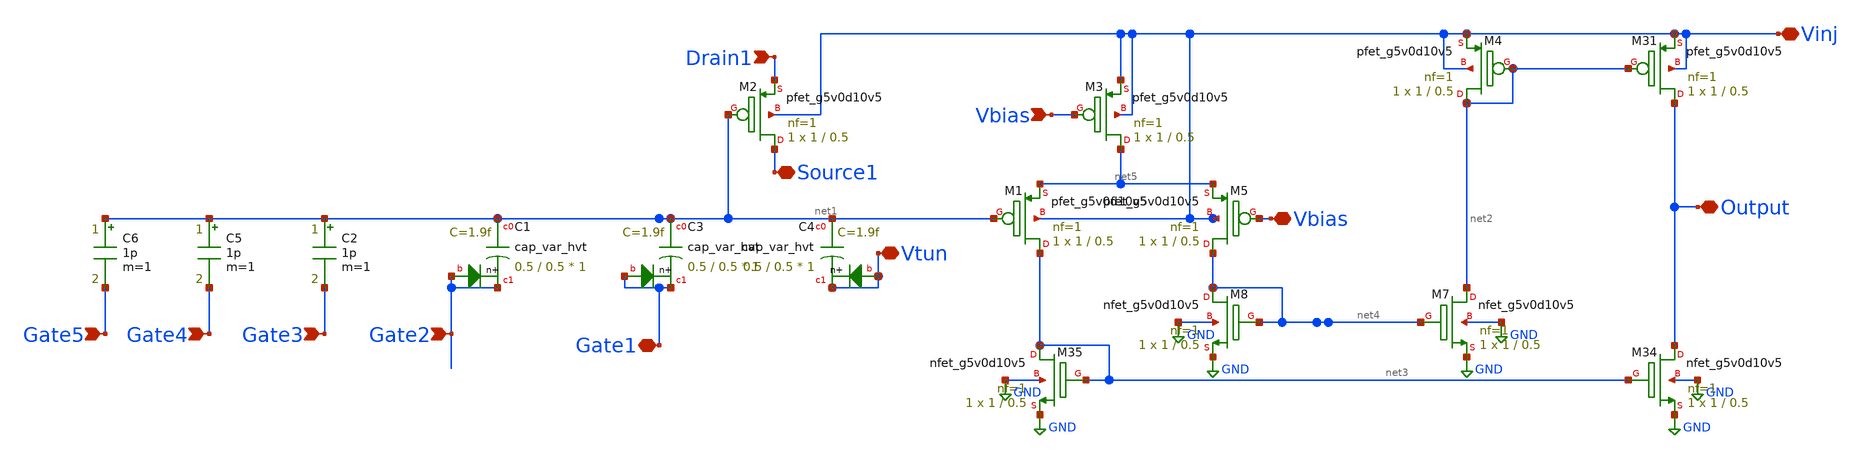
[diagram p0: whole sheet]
** sch_path: libs.ref/sky130_hilas_sc/xschem/sky130_hilas_FGcharacterization01.sch
**.subckt sky130_hilas_FGcharacterization01 Vbias Drain1 Gate3 Gate2 Vtun Source1 Vinj Gate1 Output
*+ Vbias Gate4 Gate5
*.ipin Vbias
*.ipin Drain1
*.ipin Gate3
*.ipin Gate2
*.iopin Vtun
*.iopin Source1
*.iopin Vinj
*.iopin Gate1
*.iopin Output
*.iopin Vbias
*.ipin Gate4
*.ipin Gate5
XM3 net5 Vbias Vinj Vinj sky130_fd_pr__pfet_g5v0d10v5 L=0.5 W=1 nf=1 ad='int((nf+1)/2) * W/nf * 0.29'
+ as='int((nf+2)/2) * W/nf * 0.29' pd='2*int((nf+1)/2) * (W/nf + 0.29)' ps='2*int((nf+2)/2) * (W/nf + 0.29)'
+ nrd='0.29 / W' nrs='0.29 / W' sa=0 sb=0 sd=0 mult=1 m=1
XC1 net1 Gate2 Gate2 sky130_fd_pr__cap_var_hvt W=0.5 L=0.5 VM=1 m=1
XM5 net4 Vbias net5 Vinj sky130_fd_pr__pfet_g5v0d10v5 L=0.5 W=1 nf=1 ad='int((nf+1)/2) * W/nf * 0.29'
+ as='int((nf+2)/2) * W/nf * 0.29' pd='2*int((nf+1)/2) * (W/nf + 0.29)' ps='2*int((nf+2)/2) * (W/nf + 0.29)'
+ nrd='0.29 / W' nrs='0.29 / W' sa=0 sb=0 sd=0 mult=1 m=1
XM1 net3 net1 net5 Vinj sky130_fd_pr__pfet_g5v0d10v5 L=0.5 W=1 nf=1 ad='int((nf+1)/2) * W/nf * 0.29'
+ as='int((nf+2)/2) * W/nf * 0.29' pd='2*int((nf+1)/2) * (W/nf + 0.29)' ps='2*int((nf+2)/2) * (W/nf + 0.29)'
+ nrd='0.29 / W' nrs='0.29 / W' sa=0 sb=0 sd=0 mult=1 m=1
XM2 Source1 net1 Drain1 Vinj sky130_fd_pr__pfet_g5v0d10v5 L=0.5 W=1 nf=1 ad='int((nf+1)/2) * W/nf * 0.29'
+ as='int((nf+2)/2) * W/nf * 0.29' pd='2*int((nf+1)/2) * (W/nf + 0.29)' ps='2*int((nf+2)/2) * (W/nf + 0.29)'
+ nrd='0.29 / W' nrs='0.29 / W' sa=0 sb=0 sd=0 mult=1 m=1
XC3 net1 Gate1 Gate1 sky130_fd_pr__cap_var_hvt W=0.5 L=0.5 VM=1 m=1
XM4 net2 net2 Vinj Vinj sky130_fd_pr__pfet_g5v0d10v5 L=0.5 W=1 nf=1 ad='int((nf+1)/2) * W/nf * 0.29'
+ as='int((nf+2)/2) * W/nf * 0.29' pd='2*int((nf+1)/2) * (W/nf + 0.29)' ps='2*int((nf+2)/2) * (W/nf + 0.29)'
+ nrd='0.29 / W' nrs='0.29 / W' sa=0 sb=0 sd=0 mult=1 m=1
XC4 net1 Vtun Vtun sky130_fd_pr__cap_var_hvt W=0.5 L=0.5 VM=1 m=1
XM31 Output net2 Vinj Vinj sky130_fd_pr__pfet_g5v0d10v5 L=0.5 W=1 nf=1 ad='int((nf+1)/2) * W/nf * 0.29'
+ as='int((nf+2)/2) * W/nf * 0.29' pd='2*int((nf+1)/2) * (W/nf + 0.29)' ps='2*int((nf+2)/2) * (W/nf + 0.29)'
+ nrd='0.29 / W' nrs='0.29 / W' sa=0 sb=0 sd=0 mult=1 m=1
XM34 Output net3 GND GND sky130_fd_pr__nfet_g5v0d10v5 L=0.5 W=1 nf=1 ad='int((nf+1)/2) * W/nf * 0.29'
+ as='int((nf+2)/2) * W/nf * 0.29' pd='2*int((nf+1)/2) * (W/nf + 0.29)' ps='2*int((nf+2)/2) * (W/nf + 0.29)'
+ nrd='0.29 / W' nrs='0.29 / W' sa=0 sb=0 sd=0 mult=1 m=1
XM35 net3 net3 GND GND sky130_fd_pr__nfet_g5v0d10v5 L=0.5 W=1 nf=1 ad='int((nf+1)/2) * W/nf * 0.29' as='int((nf+2)/2) * W/nf * 0.29'
+ pd='2*int((nf+1)/2) * (W/nf + 0.29)' ps='2*int((nf+2)/2) * (W/nf + 0.29)' nrd='0.29 / W' nrs='0.29 / W'
+ sa=0 sb=0 sd=0 mult=1 m=1
XM7 net2 net4 GND GND sky130_fd_pr__nfet_g5v0d10v5 L=0.5 W=1 nf=1 ad='int((nf+1)/2) * W/nf * 0.29' as='int((nf+2)/2) * W/nf * 0.29'
+ pd='2*int((nf+1)/2) * (W/nf + 0.29)' ps='2*int((nf+2)/2) * (W/nf + 0.29)' nrd='0.29 / W' nrs='0.29 / W'
+ sa=0 sb=0 sd=0 mult=1 m=1
XM8 net4 net4 GND GND sky130_fd_pr__nfet_g5v0d10v5 L=0.5 W=1 nf=1 ad='int((nf+1)/2) * W/nf * 0.29' as='int((nf+2)/2) * W/nf * 0.29'
+ pd='2*int((nf+1)/2) * (W/nf + 0.29)' ps='2*int((nf+2)/2) * (W/nf + 0.29)' nrd='0.29 / W' nrs='0.29 / W'
+ sa=0 sb=0 sd=0 mult=1 m=1
C2 net1 Gate3 1p m=1
C5 net1 Gate4 1p m=1
C6 net1 Gate5 1p m=1
**.ends
.GLOBAL GND
.end
